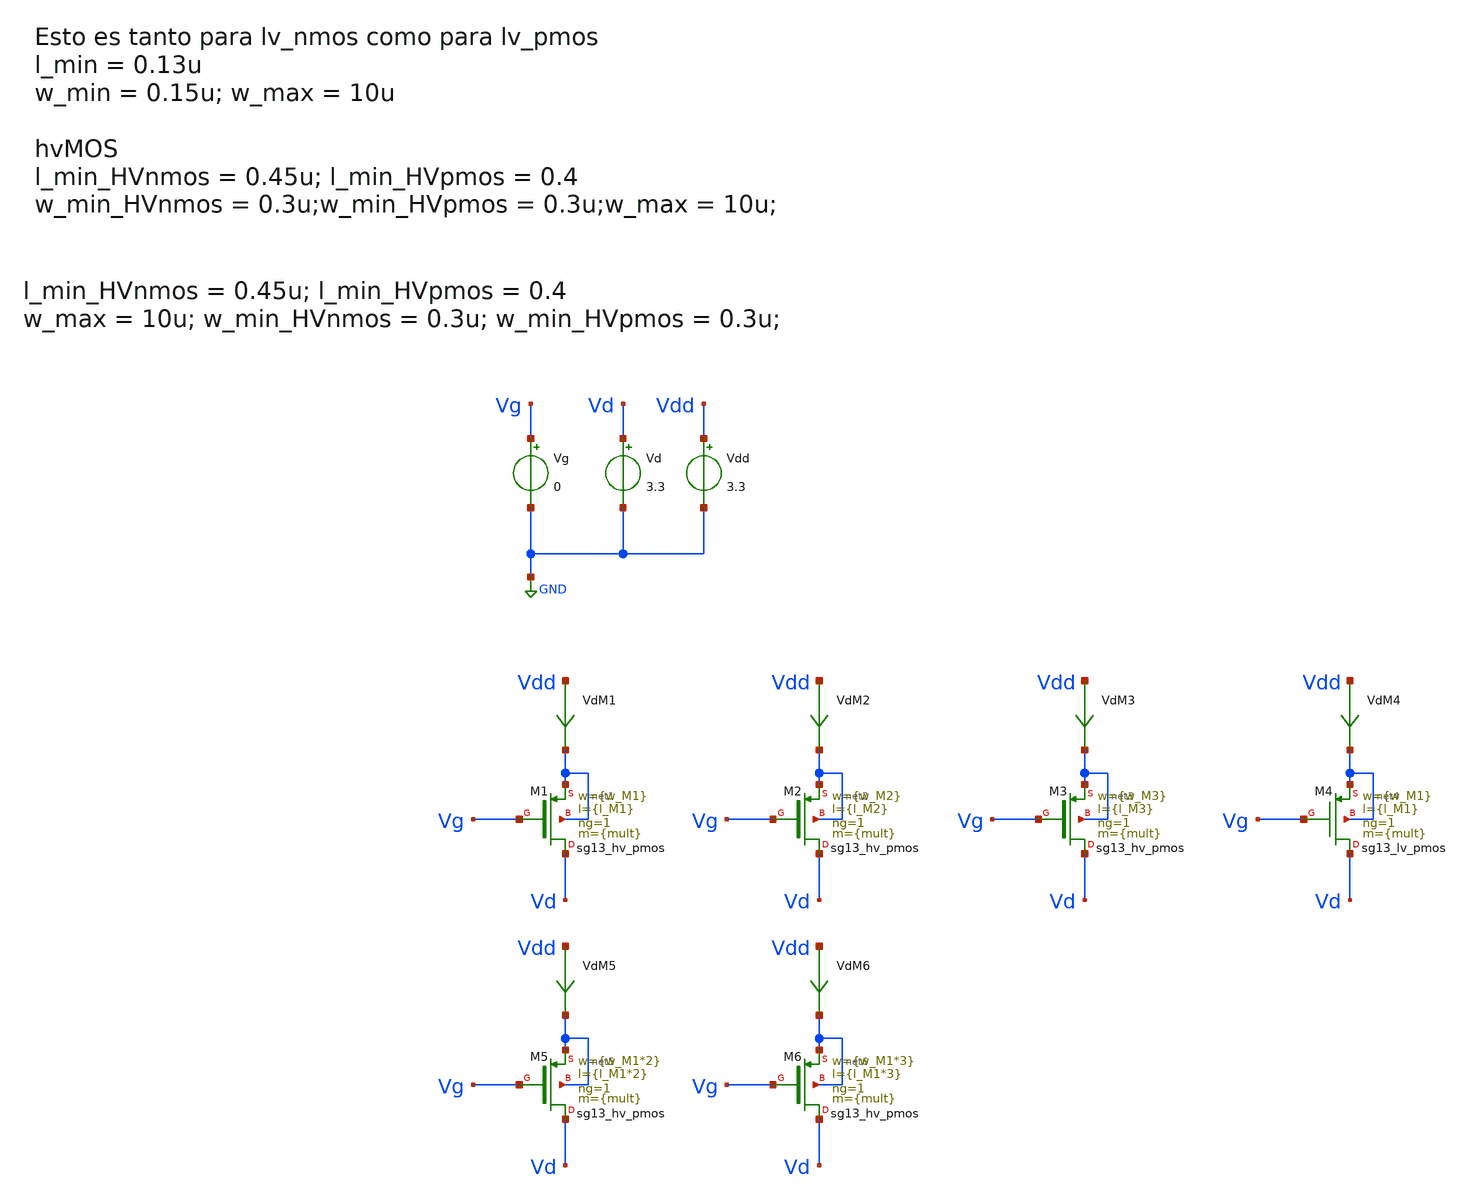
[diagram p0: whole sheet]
** sch_path: ChipUSM_AnalogTrack24/TestBenchs/TB_hvPMOS_charact.sch
**.subckt TB_hvPMOS_charact
XM1 Vd Vg net1 net1 sg13_hv_pmos w={w_M1} l={l_M1} ng=1 m={mult} mm_ok=1
Vg Vg GND 0
Vd Vd GND 3.3
Vdd Vdd GND 3.3
VdM1 Vdd net1 0
.save i(vdm1)
XM2 Vd Vg net2 net2 sg13_hv_pmos w={w_M2} l={l_M2} ng=1 m={mult} mm_ok=1
VdM2 Vdd net2 0
.save i(vdm2)
XM3 Vd Vg net3 net3 sg13_hv_pmos w={w_M3} l={l_M3} ng=1 m={mult} mm_ok=1
VdM3 Vdd net3 0
.save i(vdm3)
XM4 Vd Vg net4 net4 sg13_lv_pmos w={w_M1} l={l_M1} ng=1 m={mult} mm_ok=1
VdM4 Vdd net4 0
.save i(vdm4)
XM5 Vd Vg net5 net5 sg13_hv_pmos w={w_M1*2} l={l_M1*2} ng=1 m={mult} mm_ok=1
VdM5 Vdd net5 0
.save i(vdm5)
XM6 Vd Vg net6 net6 sg13_hv_pmos w={w_M1*3} l={l_M1*3} ng=1 m={mult} mm_ok=1
VdM6 Vdd net6 0
.save i(vdm6)
**** begin user architecture code



*.option temp= 27
.option temp= 125

.param mult = 1

.param w_M1 =10u
.param l_M1 =0.4u

.param w_M2 =10u
.param l_M2 =0.45u

.param w_M3 =10u
.param l_M3 =0.5u

.save all  @n.xm1.nsg13_hv_pmos[vth]  @n.xm1.nsg13_hv_pmos[gds]  @n.xm2.nsg13_hv_pmos[vth]  @n.xm2.nsg13_hv_pmos[gds]  @n.xm3.nsg13_hv_pmos[vth]  @n.xm3.nsg13_hv_pmos[gds]  @n.xm4.nsg13_lv_pmos[vth]  @n.xm4.nsg13_lv_pmos[gds]  @n.xm5.nsg13_hv_pmos[vth]  @n.xm5.nsg13_hv_pmos[gds]  @n.xm6.nsg13_hv_pmos[vth]  @n.xm6.nsg13_hv_pmos[gds]
.control

*alter Vdd 5

*dc Vd 0 3.3 0.01 Vg 0.5 3.3 0.5
*dc Vd 0 0.5 0.01 temp 0 27 1
dc Vd 0 3.3 0.01

let Vsd = v(Vdd) - v(Vd)
let G_M1 = @n.xm1.nsg13_hv_pmos[gds]
let G_M2 = @n.xm2.nsg13_hv_pmos[gds]
let G_M3 = @n.xm3.nsg13_hv_pmos[gds]
let G_M4 = @n.xm4.nsg13_lv_pmos[gds]
let G_M5 = @n.xm5.nsg13_hv_pmos[gds]
let G_M6 = @n.xm6.nsg13_hv_pmos[gds]
let Ron_M1 = 1/G_M1
let Ron_M2 = 1/G_M2
let Ron_M3 = 1/G_M3
let Ron_M4 = 1/G_M4
let Ron_M5 = 1/G_M5
let Ron_M6 = 1/G_M6

plot i(VdM1) i(VdM2) i(VdM3) vs Vsd
plot i(VdM1) i(VdM4) vs Vsd
plot i(VdM1) i(VdM5) i(VdM6) vs Vsd
plot Ron_M1 Ron_M2 Ron_M3 vs Vsd
plot Ron_M1 Ron_M4 vs Vsd
plot Ron_M1 Ron_M5 Ron_M6 vs Vsd
*plot i(VdM1) i(VdM2) vs Vsd

*plot @n.xm1.nsg13_hv_pmos[vth] @n.xm2.nsg13_hv_pmos[vth] @n.xm3.nsg13_hv_pmos[vth]
*print @n.xm2.nsg13_hv_nmos[vth]
write test_pmos.raw
.endc


.control
reset
alter Vd 0
dc Vg 2 3.3 0.01
let Vsg = v(Vdd) - v(Vg)
plot i(VdM1) i(VdM2) i(VdM3) vs Vsg
.endc




.lib cornerMOShv.lib mos_tt
.lib cornerMOSlv.lib mos_tt
*.lib cornerMOShv.lib mos_ss
*.lib cornerMOShv.lib mos_ff
*.lib cornerMOShv.lib mos_sf
*.lib cornerMOShv.lib mos_fs

**** end user architecture code
**.ends
.GLOBAL GND
.end
